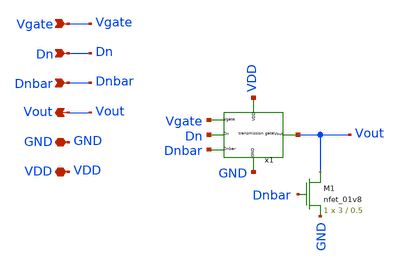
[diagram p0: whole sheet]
** sch_path: final/LDS/gate_driver_LDS.sch
**.subckt gate_driver_LDS Vgate Dn Vout Dnbar GND VDD
*.ipin Vgate
*.ipin Dn
*.opin Vout
*.ipin Dnbar
*.iopin GND
*.iopin VDD
XM1 Vout Dnbar GND GND sky130_fd_pr__nfet_01v8 L=0.5 W=3 nf=1 ad='int((nf+1)/2) * W/nf * 0.29' as='int((nf+2)/2) * W/nf * 0.29'
+ pd='2*int((nf+1)/2) * (W/nf + 0.29)' ps='2*int((nf+2)/2) * (W/nf + 0.29)' nrd='0.29 / W' nrs='0.29 / W'
+ sa=0 sb=0 sd=0 mult=1 m=1
x1 Vgate Dn Dnbar Vout VDD GND transmission_gate_LDS
**.ends
.end
